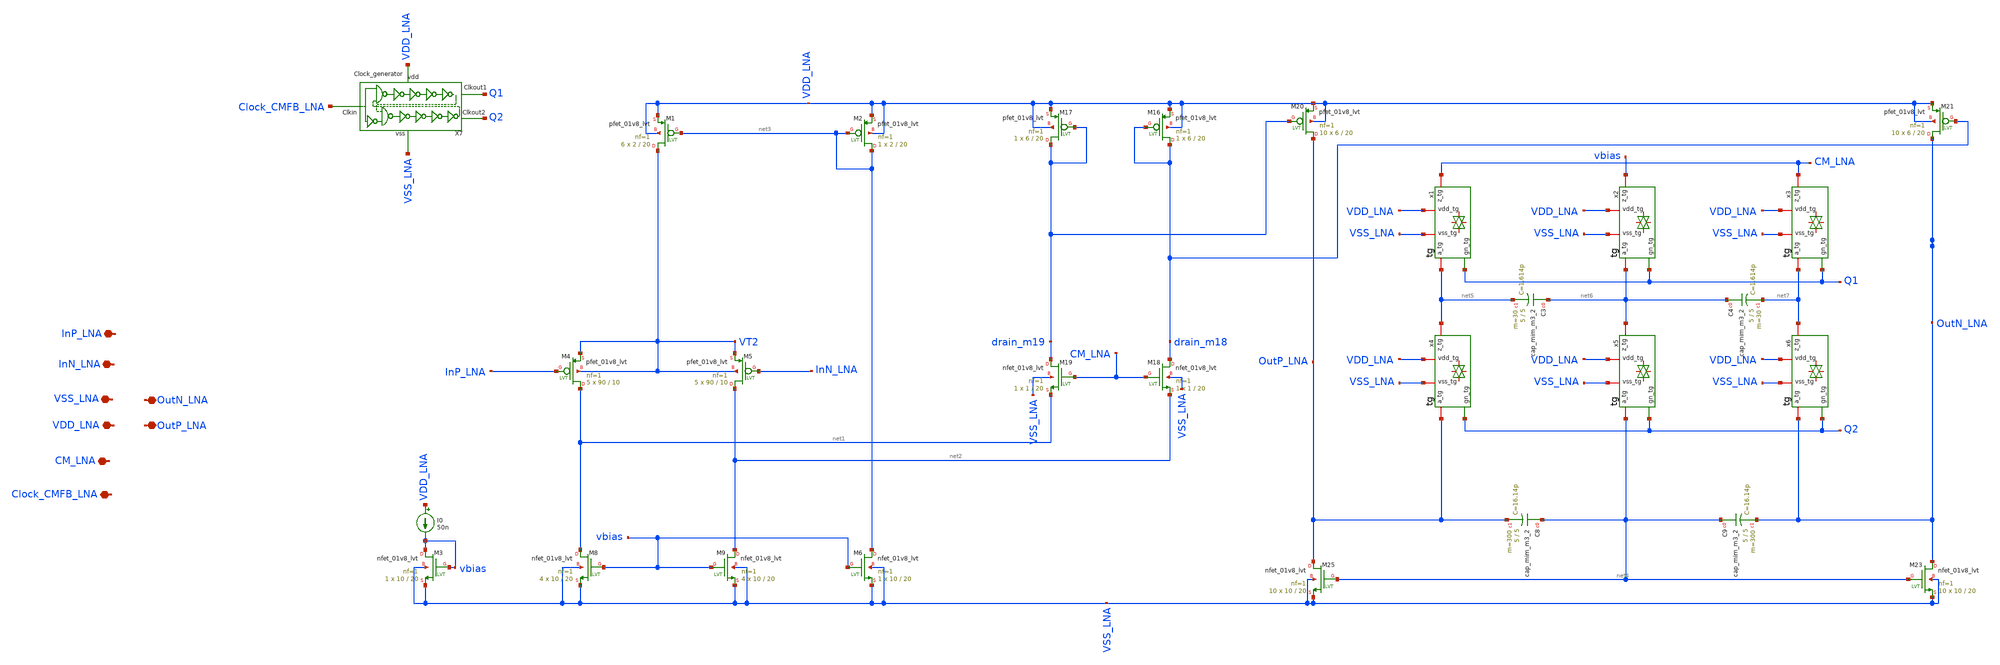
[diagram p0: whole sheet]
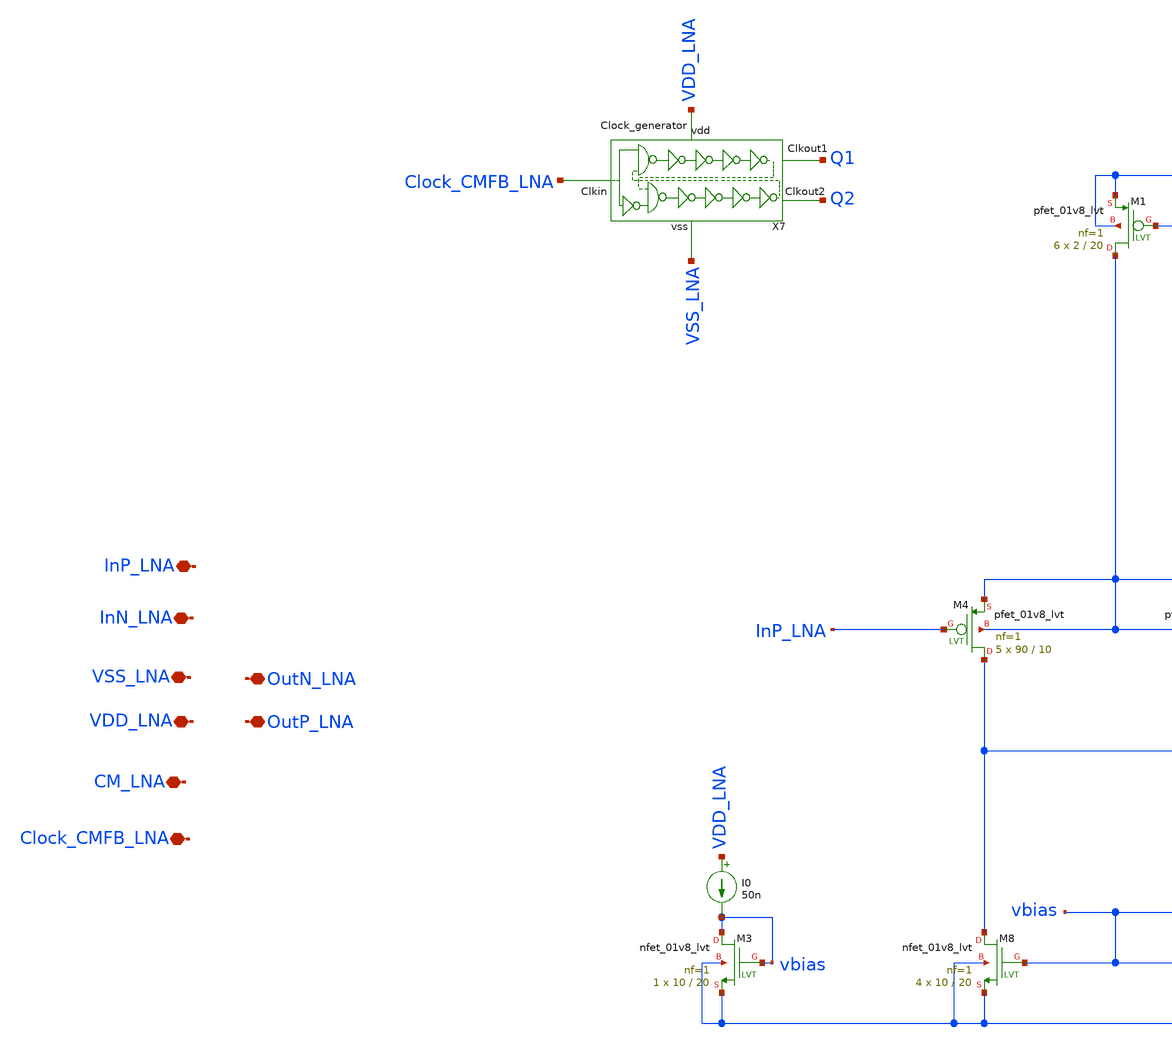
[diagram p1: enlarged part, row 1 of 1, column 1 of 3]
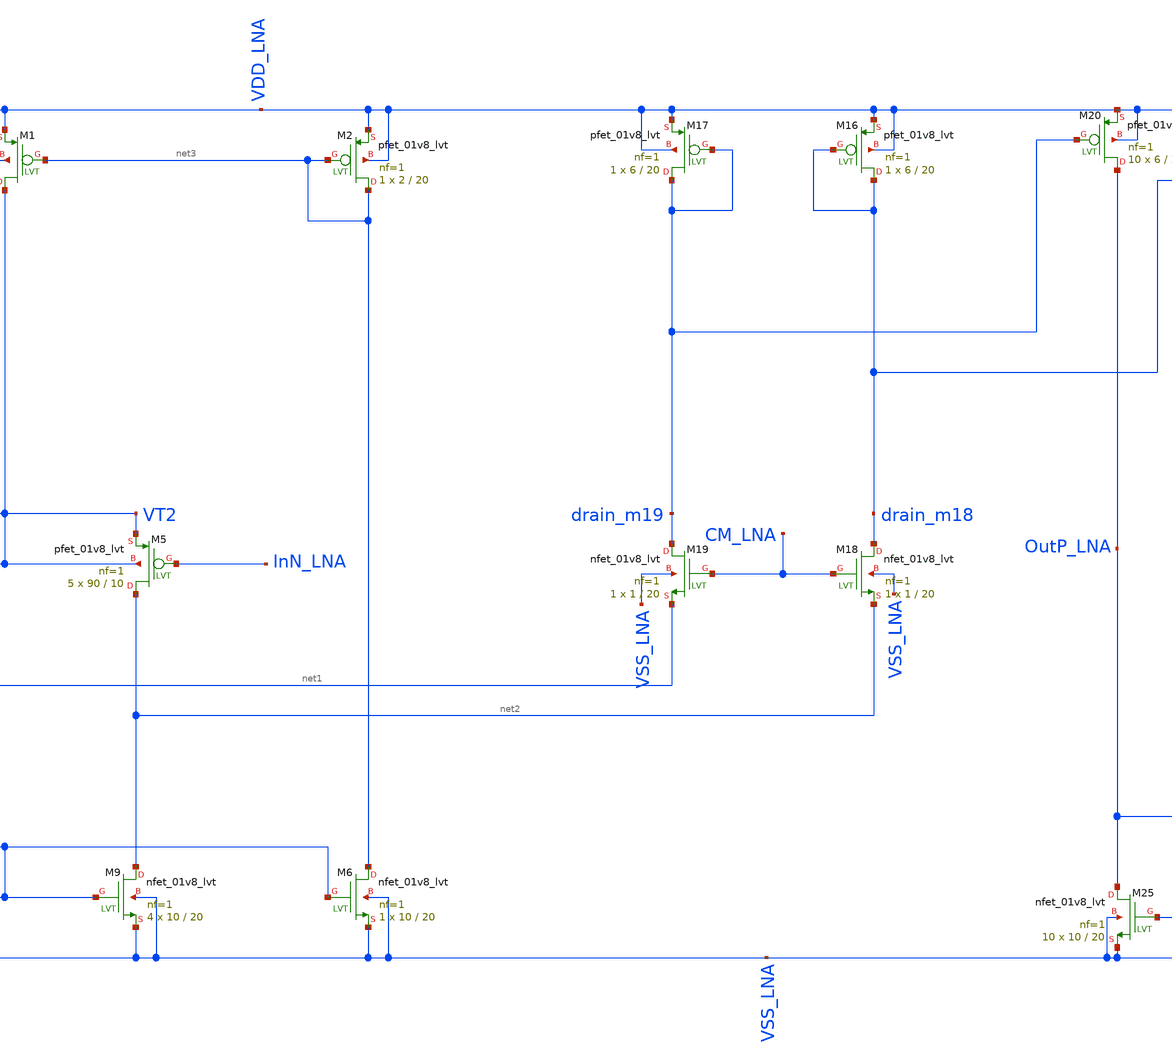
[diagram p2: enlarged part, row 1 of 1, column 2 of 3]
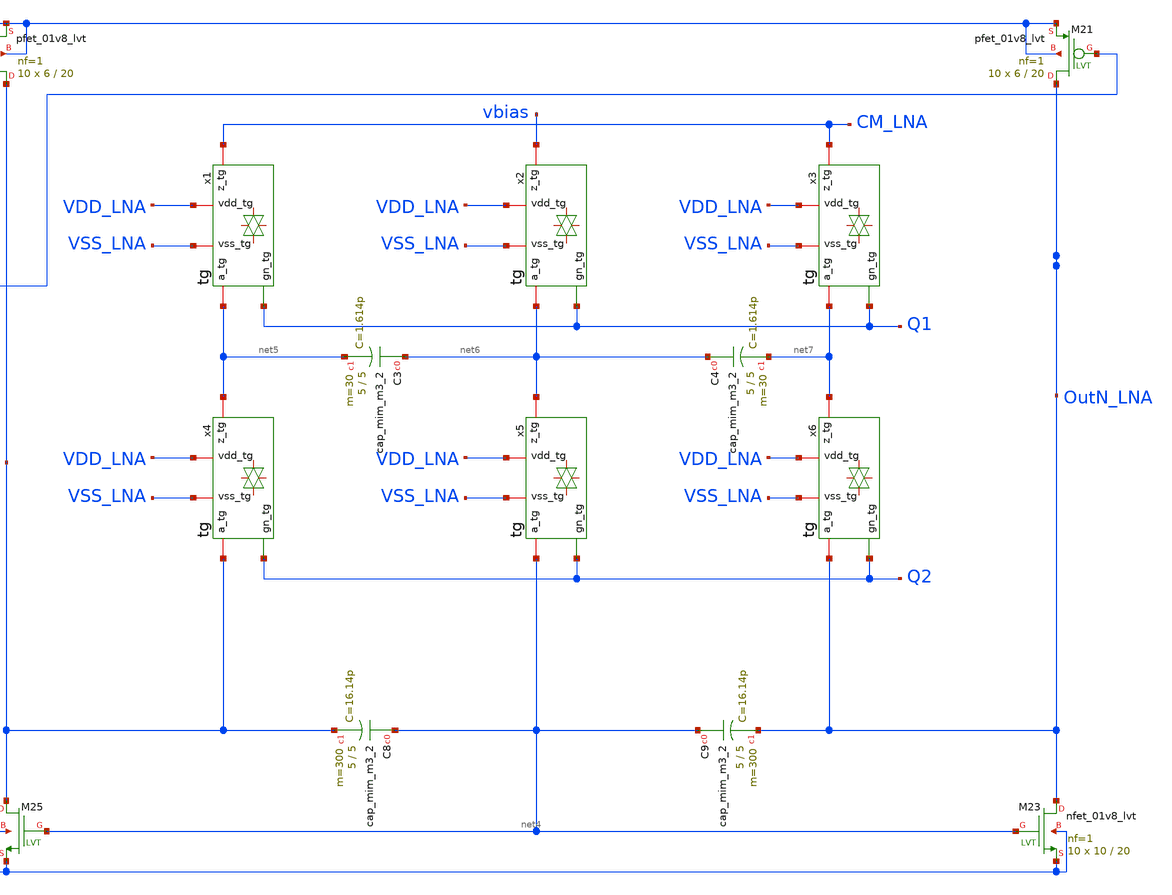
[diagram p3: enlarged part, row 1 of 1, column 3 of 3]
** sch_path: LNA.sch
**.subckt LNA InP_LNA InN_LNA VSS_LNA VDD_LNA CM_LNA OutP_LNA OutN_LNA Clock_CMFB_LNA
*.iopin InP_LNA
*.iopin InN_LNA
*.iopin VSS_LNA
*.iopin VDD_LNA
*.iopin CM_LNA
*.iopin OutP_LNA
*.iopin OutN_LNA
*.iopin Clock_CMFB_LNA
XM4 net1 InP_LNA VT2 VT2 sky130_fd_pr__pfet_01v8_lvt L=10 W=90 nf=1 ad='int((nf+1)/2) * W/nf * 0.29'
+ as='int((nf+2)/2) * W/nf * 0.29' pd='2*int((nf+1)/2) * (W/nf + 0.29)' ps='2*int((nf+2)/2) * (W/nf + 0.29)'
+ nrd='0.29 / W' nrs='0.29 / W' sa=0 sb=0 sd=0 mult=5 m=5
XM5 net2 InN_LNA VT2 VT2 sky130_fd_pr__pfet_01v8_lvt L=10 W=90 nf=1 ad='int((nf+1)/2) * W/nf * 0.29'
+ as='int((nf+2)/2) * W/nf * 0.29' pd='2*int((nf+1)/2) * (W/nf + 0.29)' ps='2*int((nf+2)/2) * (W/nf + 0.29)'
+ nrd='0.29 / W' nrs='0.29 / W' sa=0 sb=0 sd=0 mult=5 m=5
XM8 net1 vbias VSS_LNA VSS_LNA sky130_fd_pr__nfet_01v8_lvt L=20 W=10 nf=1 ad='int((nf+1)/2) * W/nf * 0.29'
+ as='int((nf+2)/2) * W/nf * 0.29' pd='2*int((nf+1)/2) * (W/nf + 0.29)' ps='2*int((nf+2)/2) * (W/nf + 0.29)'
+ nrd='0.29 / W' nrs='0.29 / W' sa=0 sb=0 sd=0 mult=4 m=4
XM9 net2 vbias VSS_LNA VSS_LNA sky130_fd_pr__nfet_01v8_lvt L=20 W=10 nf=1 ad='int((nf+1)/2) * W/nf * 0.29'
+ as='int((nf+2)/2) * W/nf * 0.29' pd='2*int((nf+1)/2) * (W/nf + 0.29)' ps='2*int((nf+2)/2) * (W/nf + 0.29)'
+ nrd='0.29 / W' nrs='0.29 / W' sa=0 sb=0 sd=0 mult=4 m=4
XM16 drain_m18 drain_m18 VDD_LNA VDD_LNA sky130_fd_pr__pfet_01v8_lvt L=20 W=6 nf=1 ad='int((nf+1)/2) * W/nf * 0.29'
+ as='int((nf+2)/2) * W/nf * 0.29' pd='2*int((nf+1)/2) * (W/nf + 0.29)' ps='2*int((nf+2)/2) * (W/nf + 0.29)'
+ nrd='0.29 / W' nrs='0.29 / W' sa=0 sb=0 sd=0 mult=1 m=1
XM17 drain_m19 drain_m19 VDD_LNA VDD_LNA sky130_fd_pr__pfet_01v8_lvt L=20 W=6 nf=1 ad='int((nf+1)/2) * W/nf * 0.29'
+ as='int((nf+2)/2) * W/nf * 0.29' pd='2*int((nf+1)/2) * (W/nf + 0.29)' ps='2*int((nf+2)/2) * (W/nf + 0.29)'
+ nrd='0.29 / W' nrs='0.29 / W' sa=0 sb=0 sd=0 mult=1 m=1
XM18 drain_m18 CM_LNA net2 VSS_LNA sky130_fd_pr__nfet_01v8_lvt L=20 W=1 nf=1 ad='int((nf+1)/2) * W/nf * 0.29'
+ as='int((nf+2)/2) * W/nf * 0.29' pd='2*int((nf+1)/2) * (W/nf + 0.29)' ps='2*int((nf+2)/2) * (W/nf + 0.29)'
+ nrd='0.29 / W' nrs='0.29 / W' sa=0 sb=0 sd=0 mult=1 m=1
XM19 drain_m19 CM_LNA net1 VSS_LNA sky130_fd_pr__nfet_01v8_lvt L=20 W=1 nf=1 ad='int((nf+1)/2) * W/nf * 0.29'
+ as='int((nf+2)/2) * W/nf * 0.29' pd='2*int((nf+1)/2) * (W/nf + 0.29)' ps='2*int((nf+2)/2) * (W/nf + 0.29)'
+ nrd='0.29 / W' nrs='0.29 / W' sa=0 sb=0 sd=0 mult=1 m=1
XM20 OutP_LNA drain_m19 VDD_LNA VDD_LNA sky130_fd_pr__pfet_01v8_lvt L=20 W=6 nf=1 ad='int((nf+1)/2) * W/nf * 0.29'
+ as='int((nf+2)/2) * W/nf * 0.29' pd='2*int((nf+1)/2) * (W/nf + 0.29)' ps='2*int((nf+2)/2) * (W/nf + 0.29)'
+ nrd='0.29 / W' nrs='0.29 / W' sa=0 sb=0 sd=0 mult=10 m=10
XM21 OutN_LNA drain_m18 VDD_LNA VDD_LNA sky130_fd_pr__pfet_01v8_lvt L=20 W=6 nf=1 ad='int((nf+1)/2) * W/nf * 0.29'
+ as='int((nf+2)/2) * W/nf * 0.29' pd='2*int((nf+1)/2) * (W/nf + 0.29)' ps='2*int((nf+2)/2) * (W/nf + 0.29)'
+ nrd='0.29 / W' nrs='0.29 / W' sa=0 sb=0 sd=0 mult=10 m=10
XM23 OutN_LNA net4 VSS_LNA VSS_LNA sky130_fd_pr__nfet_01v8_lvt L=20 W=10 nf=1 ad='int((nf+1)/2) * W/nf * 0.29'
+ as='int((nf+2)/2) * W/nf * 0.29' pd='2*int((nf+1)/2) * (W/nf + 0.29)' ps='2*int((nf+2)/2) * (W/nf + 0.29)'
+ nrd='0.29 / W' nrs='0.29 / W' sa=0 sb=0 sd=0 mult=10 m=10
XM25 OutP_LNA net4 VSS_LNA VSS_LNA sky130_fd_pr__nfet_01v8_lvt L=20 W=10 nf=1 ad='int((nf+1)/2) * W/nf * 0.29'
+ as='int((nf+2)/2) * W/nf * 0.29' pd='2*int((nf+1)/2) * (W/nf + 0.29)' ps='2*int((nf+2)/2) * (W/nf + 0.29)'
+ nrd='0.29 / W' nrs='0.29 / W' sa=0 sb=0 sd=0 mult=10 m=10
XM1 VT2 net3 VDD_LNA VDD_LNA sky130_fd_pr__pfet_01v8_lvt L=20 W=2 nf=1 ad='int((nf+1)/2) * W/nf * 0.29'
+ as='int((nf+2)/2) * W/nf * 0.29' pd='2*int((nf+1)/2) * (W/nf + 0.29)' ps='2*int((nf+2)/2) * (W/nf + 0.29)'
+ nrd='0.29 / W' nrs='0.29 / W' sa=0 sb=0 sd=0 mult=6 m=6
XM2 net3 net3 VDD_LNA VDD_LNA sky130_fd_pr__pfet_01v8_lvt L=20 W=2 nf=1 ad='int((nf+1)/2) * W/nf * 0.29'
+ as='int((nf+2)/2) * W/nf * 0.29' pd='2*int((nf+1)/2) * (W/nf + 0.29)' ps='2*int((nf+2)/2) * (W/nf + 0.29)'
+ nrd='0.29 / W' nrs='0.29 / W' sa=0 sb=0 sd=0 mult=1 m=1
XM6 net3 vbias VSS_LNA VSS_LNA sky130_fd_pr__nfet_01v8_lvt L=20 W=10 nf=1 ad='int((nf+1)/2) * W/nf * 0.29'
+ as='int((nf+2)/2) * W/nf * 0.29' pd='2*int((nf+1)/2) * (W/nf + 0.29)' ps='2*int((nf+2)/2) * (W/nf + 0.29)'
+ nrd='0.29 / W' nrs='0.29 / W' sa=0 sb=0 sd=0 mult=1 m=1
XC3 net6 net5 sky130_fd_pr__cap_mim_m3_2 W=5 L=5 MF=30 m=30
XC4 net6 net7 sky130_fd_pr__cap_mim_m3_2 W=5 L=5 MF=30 m=30
XC8 net4 OutP_LNA sky130_fd_pr__cap_mim_m3_2 W=5 L=5 MF=300 m=300
XC9 net4 OutN_LNA sky130_fd_pr__cap_mim_m3_2 W=5 L=5 MF=300 m=300
x1 VDD_LNA net5 CM_LNA VSS_LNA Q1 tg
x2 VDD_LNA net6 vbias VSS_LNA Q1 tg
x3 VDD_LNA net7 CM_LNA VSS_LNA Q1 tg
x4 VDD_LNA OutP_LNA net5 VSS_LNA Q2 tg
x5 VDD_LNA net4 net6 VSS_LNA Q2 tg
x6 VDD_LNA OutN_LNA net7 VSS_LNA Q2 tg
X7 Clock_CMFB_LNA VSS_LNA Q1 Q2 VDD_LNA Clock_generator
XM3 vbias vbias VSS_LNA VSS_LNA sky130_fd_pr__nfet_01v8_lvt L=20 W=10 nf=1 ad='int((nf+1)/2) * W/nf * 0.29'
+ as='int((nf+2)/2) * W/nf * 0.29' pd='2*int((nf+1)/2) * (W/nf + 0.29)' ps='2*int((nf+2)/2) * (W/nf + 0.29)'
+ nrd='0.29 / W' nrs='0.29 / W' sa=0 sb=0 sd=0 mult=1 m=1
I0 VDD_LNA vbias 50n
**.ends

* expanding   symbol:  LNA/tg.sym # of pins=5
** sym_path: tg.sym
** sch_path: tg.sch
.subckt tg vdd_tg a_tg z_tg vss_tg gn_tg
*.iopin a_tg
*.iopin z_tg
*.ipin gn_tg
*.iopin vss_tg
*.iopin vdd_tg
XM1 a_tg gn_tg z_tg vss_tg sky130_fd_pr__nfet_01v8 L=0.2 W=1 nf=1 ad='int((nf+1)/2) * W/nf * 0.29' as='int((nf+2)/2) * W/nf * 0.29'
+ pd='2*int((nf+1)/2) * (W/nf + 0.29)' ps='2*int((nf+2)/2) * (W/nf + 0.29)' nrd='0.29 / W' nrs='0.29 / W'
+ sa=0 sb=0 sd=0 mult=1 m=1
XM2 a_tg net1 z_tg vdd_tg sky130_fd_pr__pfet_01v8 L=0.2 W=2 nf=2 ad='int((nf+1)/2) * W/nf * 0.29' as='int((nf+2)/2) * W/nf * 0.29'
+ pd='2*int((nf+1)/2) * (W/nf + 0.29)' ps='2*int((nf+2)/2) * (W/nf + 0.29)' nrd='0.29 / W' nrs='0.29 / W'
+ sa=0 sb=0 sd=0 mult=1 m=1
x10 gn_tg vss_tg vss_tg vdd_tg vdd_tg net1 sky130_fd_sc_hd__inv_1
.ends


* expanding   symbol:  LNA/Clock_generator.sym # of pins=5
** sym_path: Clock_generator.sym
** sch_path: Clock_generator.sch
.subckt Clock_generator clkin vss clkout1 clkout2 vdd
*.ipin clkin
*.opin clkout1
*.opin clkout2
*.iopin vss
*.iopin vdd
x1 clkin net9 vss vss vdd vdd net1 sky130_fd_sc_hd__nand2_1
x2 net1 vss vss vdd vdd net2 sky130_fd_sc_hd__inv_1
x3 net2 vss vss vdd vdd net3 sky130_fd_sc_hd__inv_1
x4 net3 vss vss vdd vdd clkout1 sky130_fd_sc_hd__inv_1
x5 clkout1 vss vss vdd vdd net5 sky130_fd_sc_hd__inv_1
x6 clkin vss vss vdd vdd net4 sky130_fd_sc_hd__inv_1
x7 net5 net4 vss vss vdd vdd net6 sky130_fd_sc_hd__nand2_1
x19 net6 vss vss vdd vdd net7 sky130_fd_sc_hd__inv_1
x20 net7 vss vss vdd vdd net8 sky130_fd_sc_hd__inv_1
x21 net8 vss vss vdd vdd clkout2 sky130_fd_sc_hd__inv_1
x22 clkout2 vss vss vdd vdd net9 sky130_fd_sc_hd__inv_1
.ends

.end
